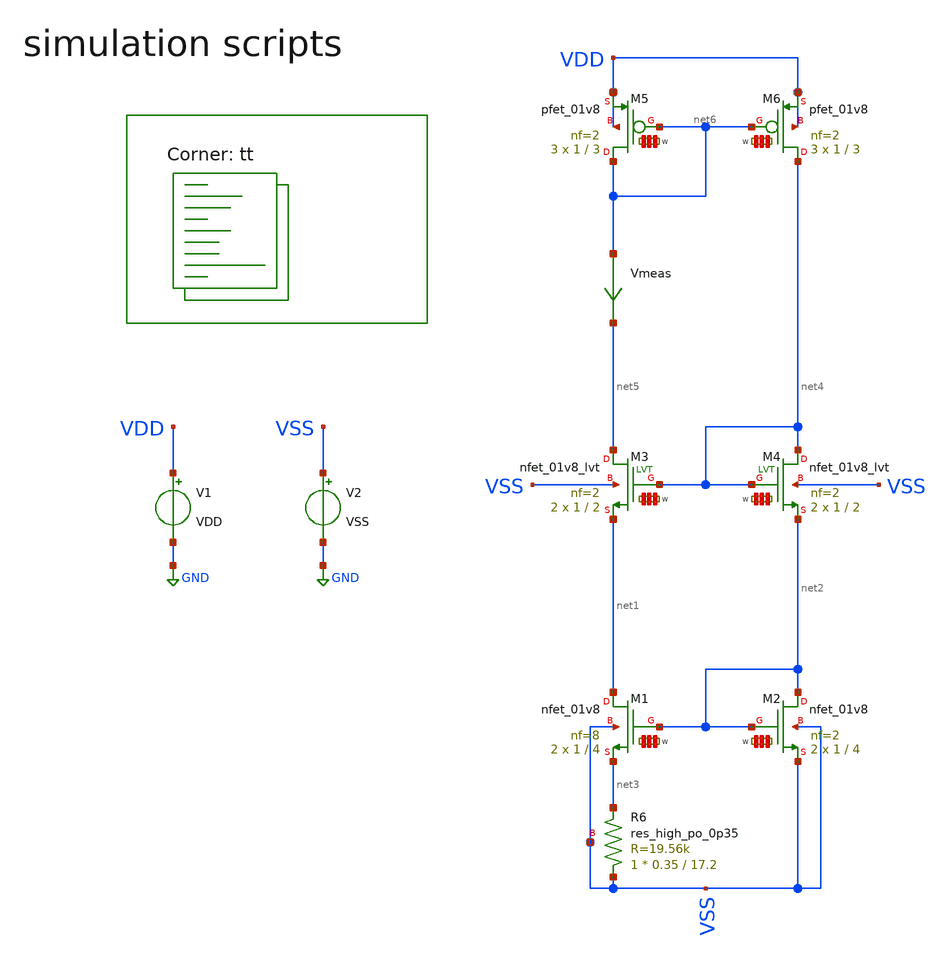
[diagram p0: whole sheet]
** sch_path: Learning/single_ended_amplifiers/VA001_series/Design_and_Analysis_of_Two-Stage_CMOS_Operational_Amplifier_for_Fluorescence_Signal_Processing_sky130_1_8V/transcondutance_cell_design/tb.sch
**.subckt tb
V1 VDD GND VDD
V2 VSS GND VSS
XR6 VSS net3 VSS sky130_fd_pr__res_high_po_0p35 L=17.2 mult=1 m=1
XM1 net1 net2 net3 VSS sky130_fd_pr__nfet_01v8 L=4 W='1 * 8 ' nf=8 ad='int((8 + 1)/2) * 1 / 8 * 0.29'
+ as='int((8 + 2)/2) * 1 / 8 * 0.29' pd='2*int((8 + 1)/2) * (1 / 8 + 0.29)' ps='2*int((8 + 2)/2) * (1 / 8 + 0.29)'
+ nrd='0.29 / 1 ' nrs='0.29 / 1 ' sa=0 sb=0 sd=0 mult=2 m=2
XM2 net2 net2 VSS VSS sky130_fd_pr__nfet_01v8 L=4 W='1 * 2 ' nf=2 ad='int((2 + 1)/2) * 1 / 2 * 0.29'
+ as='int((2 + 2)/2) * 1 / 2 * 0.29' pd='2*int((2 + 1)/2) * (1 / 2 + 0.29)' ps='2*int((2 + 2)/2) * (1 / 2 + 0.29)'
+ nrd='0.29 / 1 ' nrs='0.29 / 1 ' sa=0 sb=0 sd=0 mult=2 m=2
XM4 net4 net4 net2 VSS sky130_fd_pr__nfet_01v8_lvt L=2 W='1 * 2 ' nf=2 ad='int((2 + 1)/2) * 1 / 2 * 0.29'
+ as='int((2 + 2)/2) * 1 / 2 * 0.29' pd='2*int((2 + 1)/2) * (1 / 2 + 0.29)' ps='2*int((2 + 2)/2) * (1 / 2 + 0.29)'
+ nrd='0.29 / 1 ' nrs='0.29 / 1 ' sa=0 sb=0 sd=0 mult=2 m=2
XM3 net5 net4 net1 VSS sky130_fd_pr__nfet_01v8_lvt L=2 W='1 * 2 ' nf=2 ad='int((2 + 1)/2) * 1 / 2 * 0.29'
+ as='int((2 + 2)/2) * 1 / 2 * 0.29' pd='2*int((2 + 1)/2) * (1 / 2 + 0.29)' ps='2*int((2 + 2)/2) * (1 / 2 + 0.29)'
+ nrd='0.29 / 1 ' nrs='0.29 / 1 ' sa=0 sb=0 sd=0 mult=2 m=2
XM5 net6 net6 VDD VDD sky130_fd_pr__pfet_01v8 L=3 W='1 * 2 ' nf=2 ad= as='int((2 + 2)/2) * 1 * 0.29'
+ pd='2*int((2 + 1)/2) * (1 + 0.29)' ps='2*int((2 + 2)/2) * (1 + 0.29)' nrd='0.29 / 1 / 2 ' nrs='0.29 / 1 / 2 '
+ sa=0 sb=0 sd=0 mult=3 m=3
XM6 net4 net6 VDD VDD sky130_fd_pr__pfet_01v8 L=3 W='1 * 2 ' nf=2 ad= as='int((2 + 2)/2) * 1 * 0.29'
+ pd='2*int((2 + 1)/2) * (1 + 0.29)' ps='2*int((2 + 2)/2) * (1 + 0.29)' nrd='0.29 / 1 / 2 ' nrs='0.29 / 1 / 2 '
+ sa=0 sb=0 sd=0 mult=3 m=3
Vmeas net6 net5 0
.save i(vmeas)
**** begin user architecture code
.lib $::SKYWATER_MODELS/sky130.lib.spice tt
**** end user architecture code
**.ends
.GLOBAL GND
**** begin user architecture code




.Temp 27
.param VDD = 1.8
.param VSS = 0


.control
save all

dc Temp -40 125 1
plot i(Vmeas)



op

print @m.xm1.msky130_fd_pr__nfet_01v8[vth]
print @m.xm1.msky130_fd_pr__nfet_01v8[gm]
print 1/@m.xm1.msky130_fd_pr__nfet_01v8[gds]
print @m.xm1.msky130_fd_pr__nfet_01v8[vdsat]
print @m.xm1.msky130_fd_pr__nfet_01v8[cdg]

print @m.xm2.msky130_fd_pr__nfet_01v8[vth]
print @m.xm2.msky130_fd_pr__nfet_01v8[gm]
print 1/@m.xm2.msky130_fd_pr__nfet_01v8[gds]
print @m.xm2.msky130_fd_pr__nfet_01v8[vdsat]
print @m.xm2.msky130_fd_pr__nfet_01v8[cdg]



print @m.xm3.msky130_fd_pr__nfet_01v8_lvt[vth]
print @m.xm3.msky130_fd_pr__nfet_01v8_lvt[gm]
print 1/@m.xm3.msky130_fd_pr__nfet_01v8_lvt[gds]
print @m.xm3.msky130_fd_pr__nfet_01v8_lvt[vdsat]
print @m.xm3.msky130_fd_pr__nfet_01v8_lvt[cdg]

print @m.xm4.msky130_fd_pr__nfet_01v8_lvt[vth]
print @m.xm4.msky130_fd_pr__nfet_01v8_lvt[gm]
print 1/@m.xm4.msky130_fd_pr__nfet_01v8_lvt[gds]
print @m.xm4.msky130_fd_pr__nfet_01v8_lvt[vdsat]
print @m.xm4.msky130_fd_pr__nfet_01v8_lvt[cdg]


print @m.xm5.msky130_fd_pr__pfet_01v8[vth]
print @m.xm5.msky130_fd_pr__pfet_01v8[gm]
print 1/@m.xm5.msky130_fd_pr__pfet_01v8[gds]
print @m.xm5.msky130_fd_pr__pfet_01v8[vdsat]
print @m.xm5.msky130_fd_pr__pfet_01v8[cdg]

print @m.xm6.msky130_fd_pr__pfet_01v8[vth]
print @m.xm6.msky130_fd_pr__pfet_01v8[gm]
print 1/@m.xm6.msky130_fd_pr__pfet_01v8[gds]
print @m.xm6.msky130_fd_pr__pfet_01v8[vdsat]
print @m.xm6.msky130_fd_pr__pfet_01v8[cdg]






print i(Vmeas)

ac dec 100 1 10G
plot i(Vmeas)


.endc



**** end user architecture code
.end
